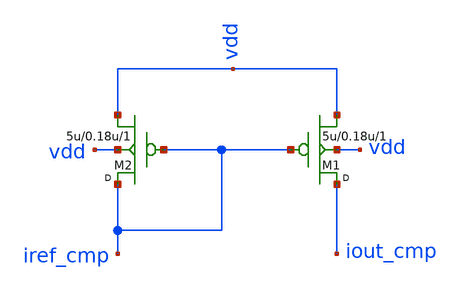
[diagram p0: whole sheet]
** sch_path: synthetic/blocks/current_mirror_pmos.sch
**.subckt current_mirror_pmos
M1 iout_cmp iref_cmp vdd vdd pmos w=5u l=0.18u m=1
M2 iref_cmp iref_cmp vdd vdd pmos w=5u l=0.18u m=1
**.ends
.end
